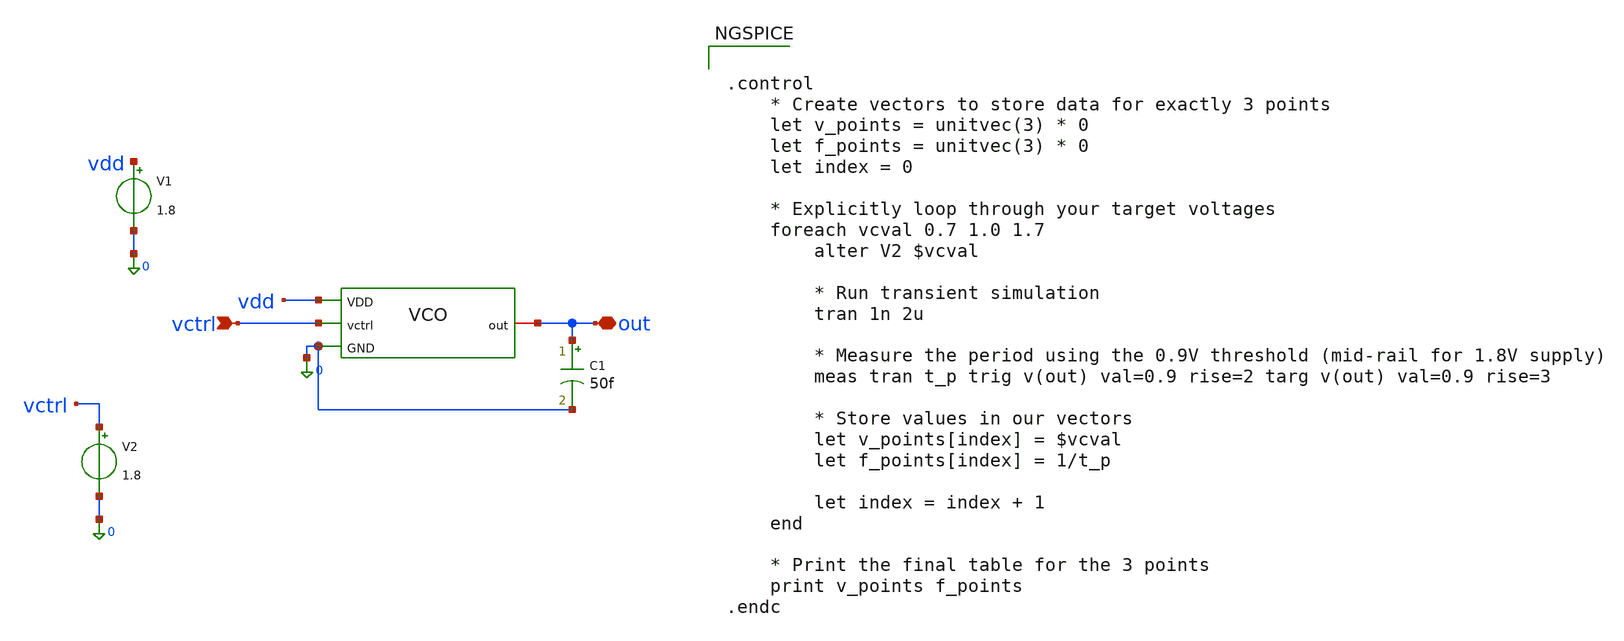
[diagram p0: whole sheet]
** sch_path: design_data/xschem/VCO/vco_tb_op.sch
**.subckt vco_tb_op vctrl out
*.ipin vctrl
*.iopin out
V1 vdd 0 1.8
V2 vctrl 0 1.8
x1 vdd out vctrl 0 vco
C1 out 0 50f m=1
**** begin user architecture code


.control
    * Create vectors to store data for exactly 3 points
    let v_points = unitvec(3) * 0
    let f_points = unitvec(3) * 0
    let index = 0

    * Explicitly loop through your target voltages
    foreach vcval 0.7 1.0 1.7
        alter V2 $vcval

        * Run transient simulation
        tran 1n 2u

        * Measure the period using the 0.9V threshold (mid-rail for 1.8V supply)
        meas tran t_p trig v(out) val=0.9 rise=2 targ v(out) val=0.9 rise=3

        * Store values in our vectors
        let v_points[index] = $vcval
        let f_points[index] = 1/t_p

        let index = index + 1
    end

    * Print the final table for the 3 points
    print v_points f_points
.endc



** opencircuitdesign pdks install
.lib $::SKYWATER_MODELS/sky130.lib.spice fs

**** end user architecture code
**.ends

* expanding   symbol:  xschem/VCO/vco.sym # of pins=4
** sym_path: xschem/VCO/vco.sym
** sch_path: xschem/VCO/vco.sch
.subckt vco VDD out vctrl GND
*.ipin vctrl
*.iopin out
*.ipin GND
*.ipin VDD
XM7 net5 net5 VDD VDD sky130_fd_pr__pfet_01v8 L=3.2 W=70 nf=1 ad='int((1 + 1)/2) * 70 / 1 * 0.29' as='int((1 + 2)/2) * 70 / 1 * 0.29'
+ pd='2*int((1 + 1)/2) * (70 / 1 + 0.29)' ps='2*int((1 + 2)/2) * (70 / 1 + 0.29)' nrd='0.29 / 70 ' nrs='0.29 / 70 '
+ sa=0 sb=0 sd=0 mult=1 m=1
XM8 net5 vctrl GND GND sky130_fd_pr__nfet_01v8 L=4.2 W=40 nf=1 ad='int((1 + 1)/2) * 40 / 1 * 0.29' as='int((1 + 2)/2) * 40 / 1 * 0.29'
+ pd='2*int((1 + 1)/2) * (40 / 1 + 0.29)' ps='2*int((1 + 2)/2) * (40 / 1 + 0.29)' nrd='0.29 / 40 ' nrs='0.29 / 40 '
+ sa=0 sb=0 sd=0 mult=1 m=1
XM5 net1 vctrl GND GND sky130_fd_pr__nfet_01v8 L=4.2 W=40 nf=1 ad='int((1 + 1)/2) * 40 / 1 * 0.29' as='int((1 + 2)/2) * 40 / 1 * 0.29'
+ pd='2*int((1 + 1)/2) * (40 / 1 + 0.29)' ps='2*int((1 + 2)/2) * (40 / 1 + 0.29)' nrd='0.29 / 40 ' nrs='0.29 / 40 '
+ sa=0 sb=0 sd=0 mult=1 m=1
XM6 net2 net4 net1 net1 sky130_fd_pr__nfet_01v8 L=1.4 W=49 nf=1 ad='int((1 + 1)/2) * 49 / 1 * 0.29' as='int((1 + 2)/2) * 49 / 1 * 0.29'
+ pd='2*int((1 + 1)/2) * (49 / 1 + 0.29)' ps='2*int((1 + 2)/2) * (49 / 1 + 0.29)' nrd='0.29 / 49 ' nrs='0.29 / 49 '
+ sa=0 sb=0 sd=0 mult=1 m=1
XM1 net3 net5 VDD VDD sky130_fd_pr__pfet_01v8 L=3.2 W=70 nf=1 ad='int((1 + 1)/2) * 70 / 1 * 0.29' as='int((1 + 2)/2) * 70 / 1 * 0.29'
+ pd='2*int((1 + 1)/2) * (70 / 1 + 0.29)' ps='2*int((1 + 2)/2) * (70 / 1 + 0.29)' nrd='0.29 / 70 ' nrs='0.29 / 70 '
+ sa=0 sb=0 sd=0 mult=1 m=1
XM2 net2 net4 net3 net3 sky130_fd_pr__pfet_01v8 L=1.4 W=74 nf=1 ad='int((1 + 1)/2) * 74 / 1 * 0.29' as='int((1 + 2)/2) * 74 / 1 * 0.29'
+ pd='2*int((1 + 1)/2) * (74 / 1 + 0.29)' ps='2*int((1 + 2)/2) * (74 / 1 + 0.29)' nrd='0.29 / 74 ' nrs='0.29 / 74 '
+ sa=0 sb=0 sd=0 mult=1 m=1
XM3 net6 vctrl GND GND sky130_fd_pr__nfet_01v8 L=4.2 W=40 nf=1 ad='int((1 + 1)/2) * 40 / 1 * 0.29' as='int((1 + 2)/2) * 40 / 1 * 0.29'
+ pd='2*int((1 + 1)/2) * (40 / 1 + 0.29)' ps='2*int((1 + 2)/2) * (40 / 1 + 0.29)' nrd='0.29 / 40 ' nrs='0.29 / 40 '
+ sa=0 sb=0 sd=0 mult=1 m=1
XM9 net7 net5 VDD VDD sky130_fd_pr__pfet_01v8 L=3.2 W=70 nf=1 ad='int((1 + 1)/2) * 70 / 1 * 0.29' as='int((1 + 2)/2) * 70 / 1 * 0.29'
+ pd='2*int((1 + 1)/2) * (70 / 1 + 0.29)' ps='2*int((1 + 2)/2) * (70 / 1 + 0.29)' nrd='0.29 / 70 ' nrs='0.29 / 70 '
+ sa=0 sb=0 sd=0 mult=1 m=1
XM11 net8 vctrl GND GND sky130_fd_pr__nfet_01v8 L=4.2 W=40 nf=1 ad='int((1 + 1)/2) * 40 / 1 * 0.29' as='int((1 + 2)/2) * 40 / 1 * 0.29'
+ pd='2*int((1 + 1)/2) * (40 / 1 + 0.29)' ps='2*int((1 + 2)/2) * (40 / 1 + 0.29)' nrd='0.29 / 40 ' nrs='0.29 / 40 '
+ sa=0 sb=0 sd=0 mult=1 m=1
XM13 net9 net5 VDD VDD sky130_fd_pr__pfet_01v8 L=3.2 W=70 nf=1 ad='int((1 + 1)/2) * 70 / 1 * 0.29' as='int((1 + 2)/2) * 70 / 1 * 0.29'
+ pd='2*int((1 + 1)/2) * (70 / 1 + 0.29)' ps='2*int((1 + 2)/2) * (70 / 1 + 0.29)' nrd='0.29 / 70 ' nrs='0.29 / 70 '
+ sa=0 sb=0 sd=0 mult=1 m=1
XM4 net10 net2 net6 net6 sky130_fd_pr__nfet_01v8 L=1.4 W=49 nf=1 ad='int((1 + 1)/2) * 49 / 1 * 0.29'
+ as='int((1 + 2)/2) * 49 / 1 * 0.29' pd='2*int((1 + 1)/2) * (49 / 1 + 0.29)' ps='2*int((1 + 2)/2) * (49 / 1 + 0.29)'
+ nrd='0.29 / 49 ' nrs='0.29 / 49 ' sa=0 sb=0 sd=0 mult=1 m=1
XM10 net10 net2 net7 net7 sky130_fd_pr__pfet_01v8 L=1.4 W=74 nf=1 ad='int((1 + 1)/2) * 74 / 1 * 0.29'
+ as='int((1 + 2)/2) * 74 / 1 * 0.29' pd='2*int((1 + 1)/2) * (74 / 1 + 0.29)' ps='2*int((1 + 2)/2) * (74 / 1 + 0.29)'
+ nrd='0.29 / 74 ' nrs='0.29 / 74 ' sa=0 sb=0 sd=0 mult=1 m=1
XM12 net4 net10 net8 net8 sky130_fd_pr__nfet_01v8 L=1.4 W=49 nf=1 ad='int((1 + 1)/2) * 49 / 1 * 0.29'
+ as='int((1 + 2)/2) * 49 / 1 * 0.29' pd='2*int((1 + 1)/2) * (49 / 1 + 0.29)' ps='2*int((1 + 2)/2) * (49 / 1 + 0.29)'
+ nrd='0.29 / 49 ' nrs='0.29 / 49 ' sa=0 sb=0 sd=0 mult=1 m=1
XM14 net4 net10 net9 net9 sky130_fd_pr__pfet_01v8 L=1.4 W=74 nf=1 ad='int((1 + 1)/2) * 74 / 1 * 0.29'
+ as='int((1 + 2)/2) * 74 / 1 * 0.29' pd='2*int((1 + 1)/2) * (74 / 1 + 0.29)' ps='2*int((1 + 2)/2) * (74 / 1 + 0.29)'
+ nrd='0.29 / 74 ' nrs='0.29 / 74 ' sa=0 sb=0 sd=0 mult=1 m=1
XM15 net11 net4 GND GND sky130_fd_pr__nfet_01v8 L=1 W=10 nf=1 ad='int((1 + 1)/2) * 10 / 1 * 0.29' as='int((1 + 2)/2) * 10 / 1 * 0.29'
+ pd='2*int((1 + 1)/2) * (10 / 1 + 0.29)' ps='2*int((1 + 2)/2) * (10 / 1 + 0.29)' nrd='0.29 / 10 ' nrs='0.29 / 10 '
+ sa=0 sb=0 sd=0 mult=1 m=1
XM16 net11 net4 VDD VDD sky130_fd_pr__pfet_01v8 L=1 W=20 nf=1 ad='int((1 + 1)/2) * 20 / 1 * 0.29' as='int((1 + 2)/2) * 20 / 1 * 0.29'
+ pd='2*int((1 + 1)/2) * (20 / 1 + 0.29)' ps='2*int((1 + 2)/2) * (20 / 1 + 0.29)' nrd='0.29 / 20 ' nrs='0.29 / 20 '
+ sa=0 sb=0 sd=0 mult=1 m=1
XM17 out net11 GND GND sky130_fd_pr__nfet_01v8 L=1 W=20 nf=1 ad='int((1 + 1)/2) * 20 / 1 * 0.29' as='int((1 + 2)/2) * 20 / 1 * 0.29'
+ pd='2*int((1 + 1)/2) * (20 / 1 + 0.29)' ps='2*int((1 + 2)/2) * (20 / 1 + 0.29)' nrd='0.29 / 20 ' nrs='0.29 / 20 '
+ sa=0 sb=0 sd=0 mult=1 m=1
XM18 out net11 VDD VDD sky130_fd_pr__pfet_01v8 L=1 W=40 nf=1 ad='int((1 + 1)/2) * 40 / 1 * 0.29' as='int((1 + 2)/2) * 40 / 1 * 0.29'
+ pd='2*int((1 + 1)/2) * (40 / 1 + 0.29)' ps='2*int((1 + 2)/2) * (40 / 1 + 0.29)' nrd='0.29 / 40 ' nrs='0.29 / 40 '
+ sa=0 sb=0 sd=0 mult=1 m=1
.ends

.end
